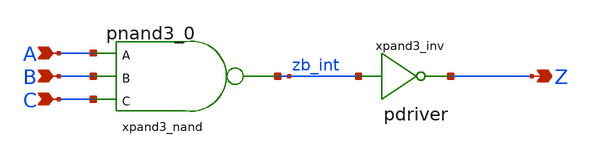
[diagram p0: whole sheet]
** sch_path: sram_4_16_scn4m/pand3.sch
**.subckt pand3 A B C Z
*.ipin A
*.ipin B
*.ipin C
*.opin Z
xpand3_nand A B C zb_int vdd gnd pnand3_0
xpand3_inv zb_int Z vdd gnd pdriver
**.ends

* expanding   symbol:  pnand3_0.sym # of pins=4
** sym_path: sram_4_16_scn4m/pnand3_0.sym
** sch_path: sram_4_16_scn4m/pnand3_0.sch
.subckt pnand3_0 A B C Z vdd gnd
*.ipin C
*.ipin A
*.ipin B
*.opin Z
*.iopin vdd
*.iopin gnd
Mpnand3_nmos1 Z C net1 gnd n w=1.6u l=0.4u m=1
Mpnand3_pmos1 Z A vdd vdd p w=1.6u l=0.4u m=1
Mpnand3_pmos3 Z C vdd vdd p w=1.6u l=0.4u m=1
Mpnand3_nmos2 net1 B net2 gnd n w=1.6u l=0.4u m=1
Mpnand3_pmos2 Z B vdd vdd p w=1.6u l=0.4u m=1
Mpnand3_nmos3 net2 A gnd gnd n w=1.6u l=0.4u m=1
.ends


* expanding   symbol:  pdriver.sym # of pins=2
** sym_path: sram_4_16_scn4m/pdriver.sym
** sch_path: sram_4_16_scn4m/pdriver.sch
.subckt pdriver A Z vdd gnd
*.ipin A
*.opin Z
xbuf_inv1 A Z vdd gnd pinv_2
.ends


* expanding   symbol:  pinv_2.sym # of pins=2
** sym_path: sram_2_64_scn4m/pinv_2.sym
** sch_path: sram_2_64_scn4m/pinv_2.sch
.subckt pinv_2 A Z vdd gnd
*.ipin A
*.opin Z
Mpinv_nmos Z A gnd gnd n w=0.8u l=0.4u m=1
Mp_inv_pmos Z A vdd vdd p w=1.6u l=0.4u m=1
.ends

.end
